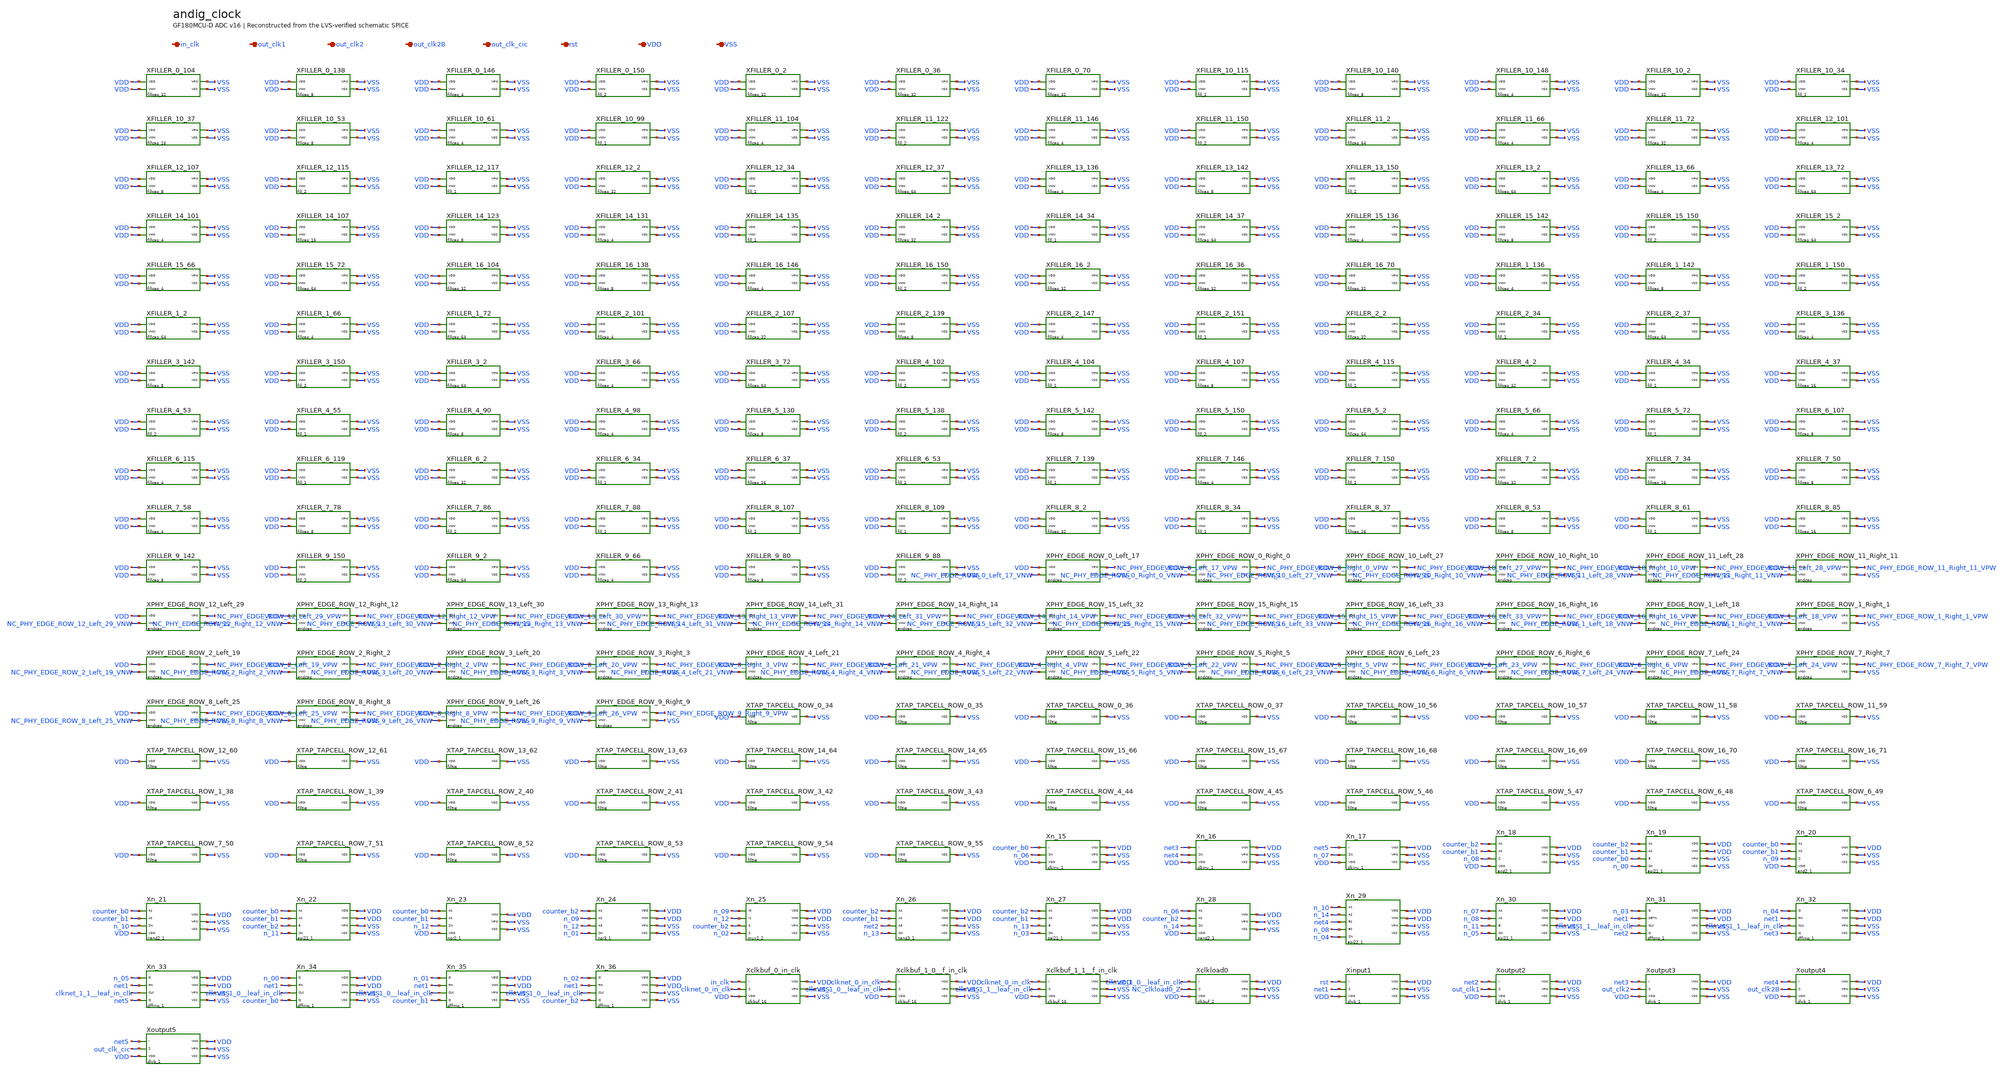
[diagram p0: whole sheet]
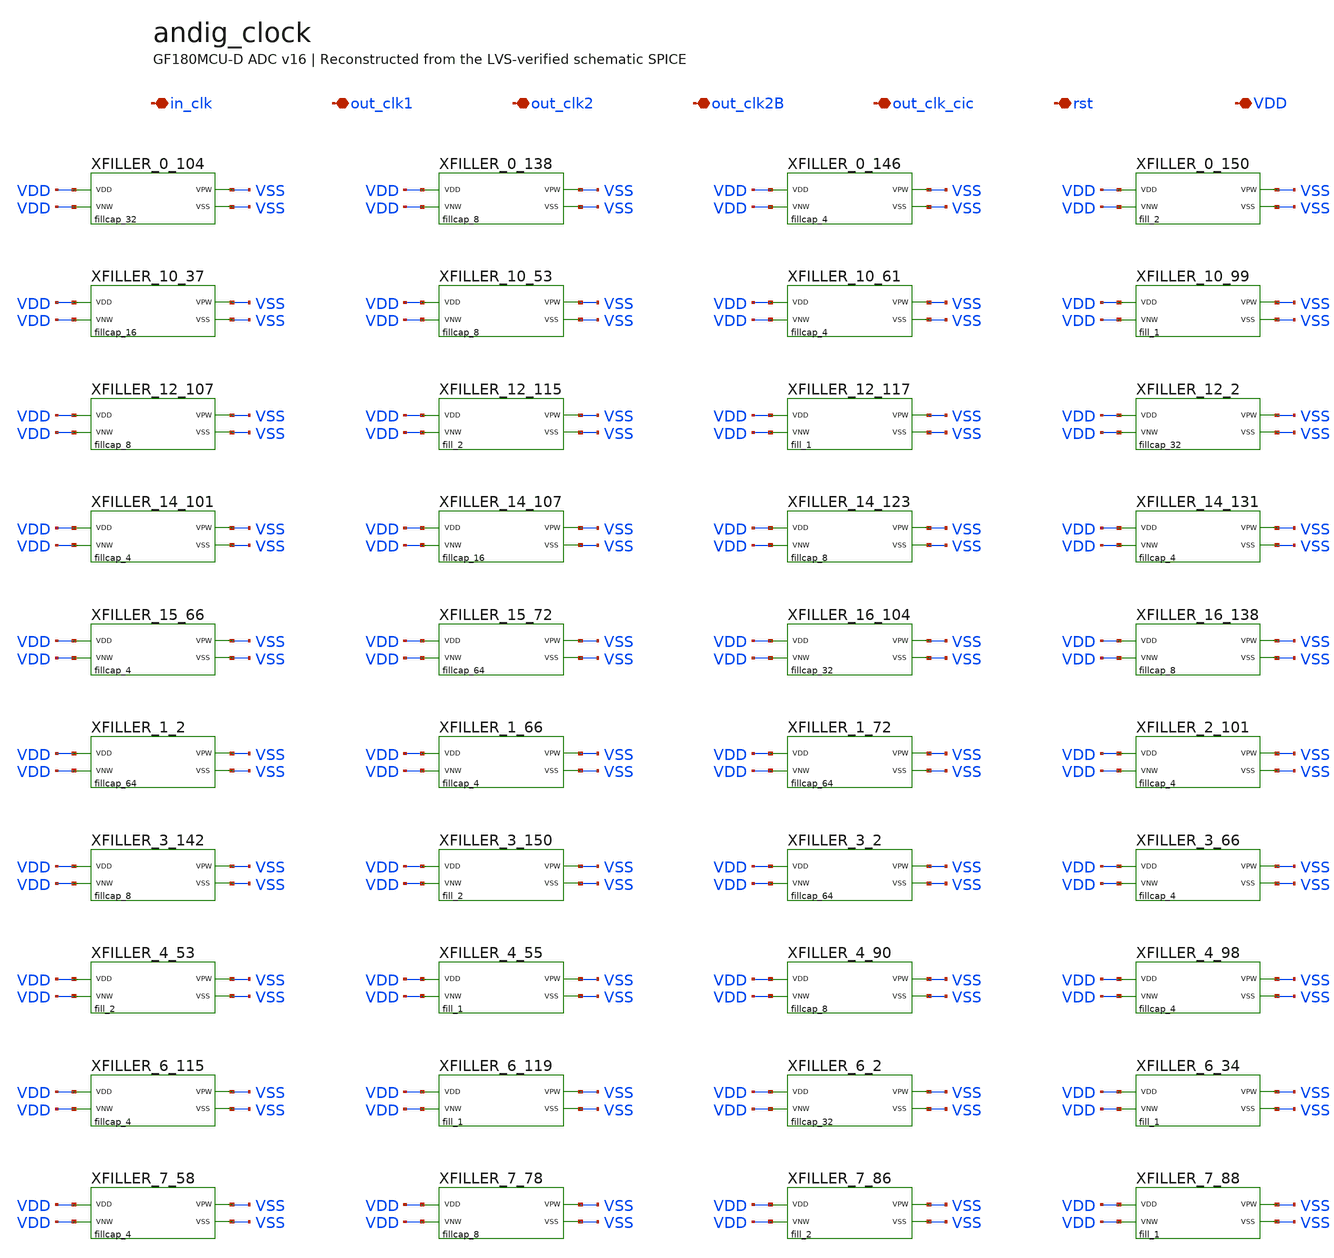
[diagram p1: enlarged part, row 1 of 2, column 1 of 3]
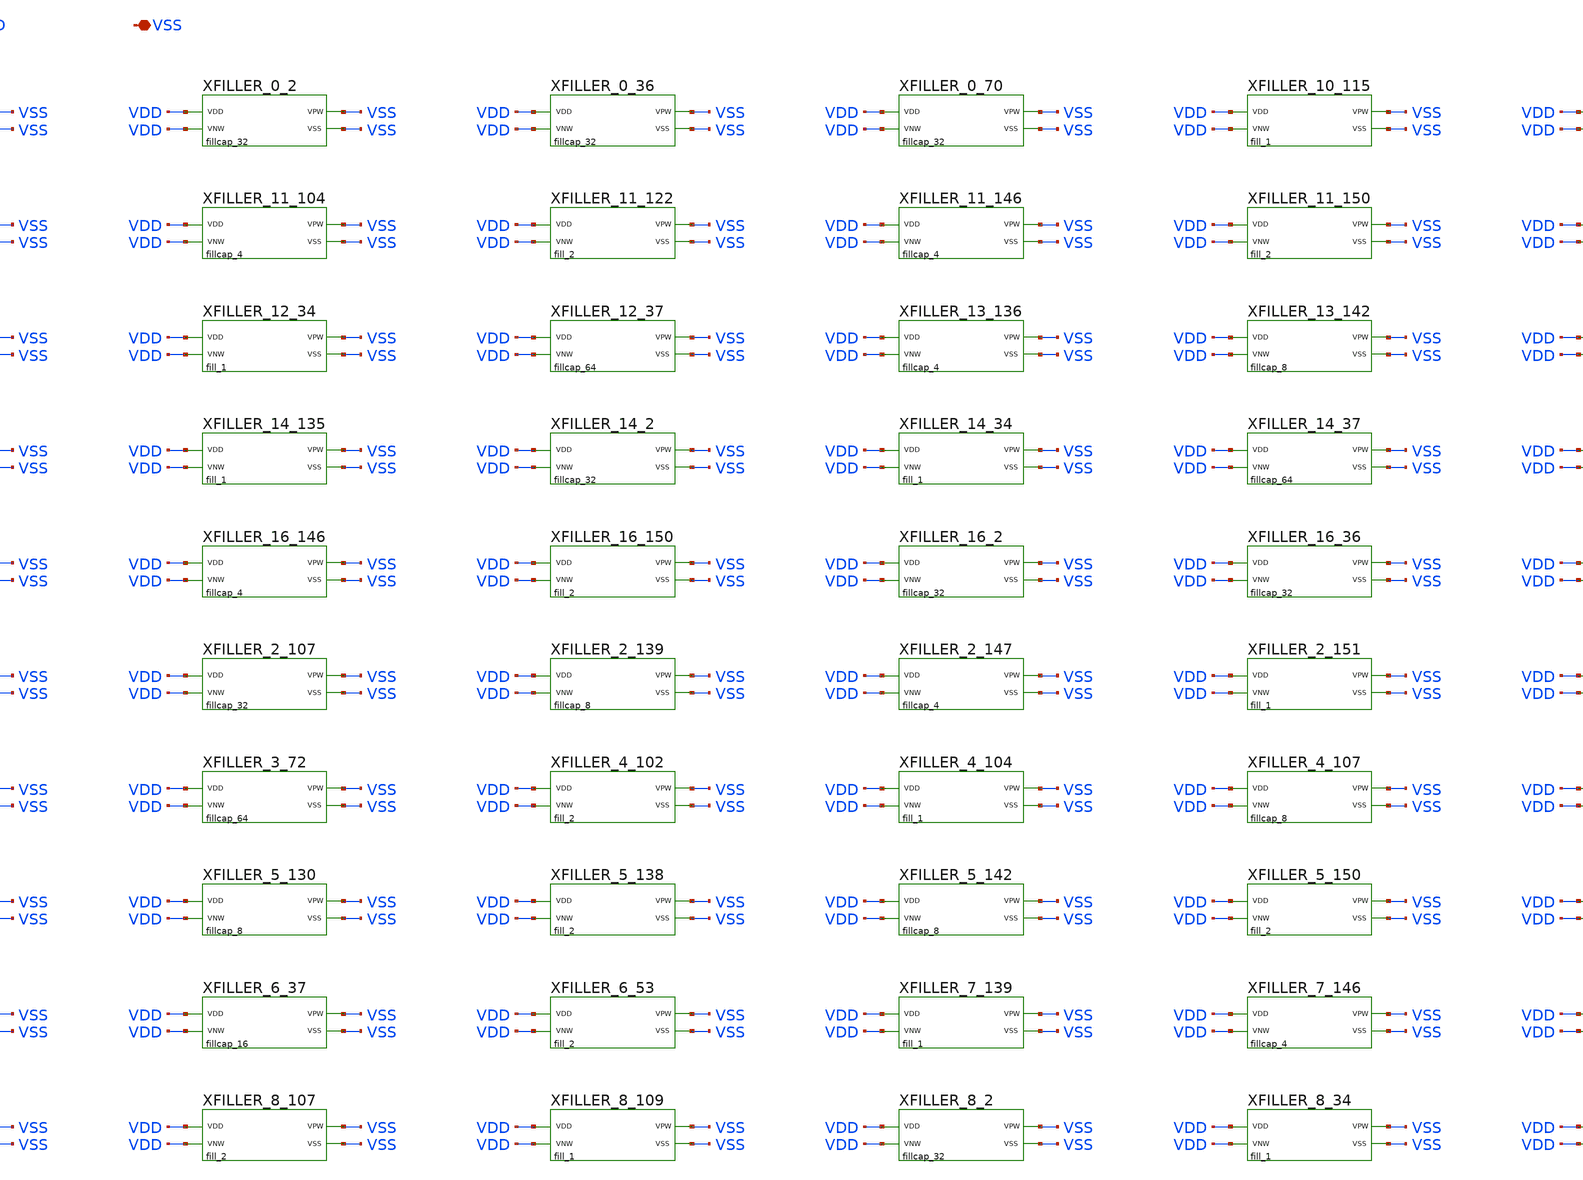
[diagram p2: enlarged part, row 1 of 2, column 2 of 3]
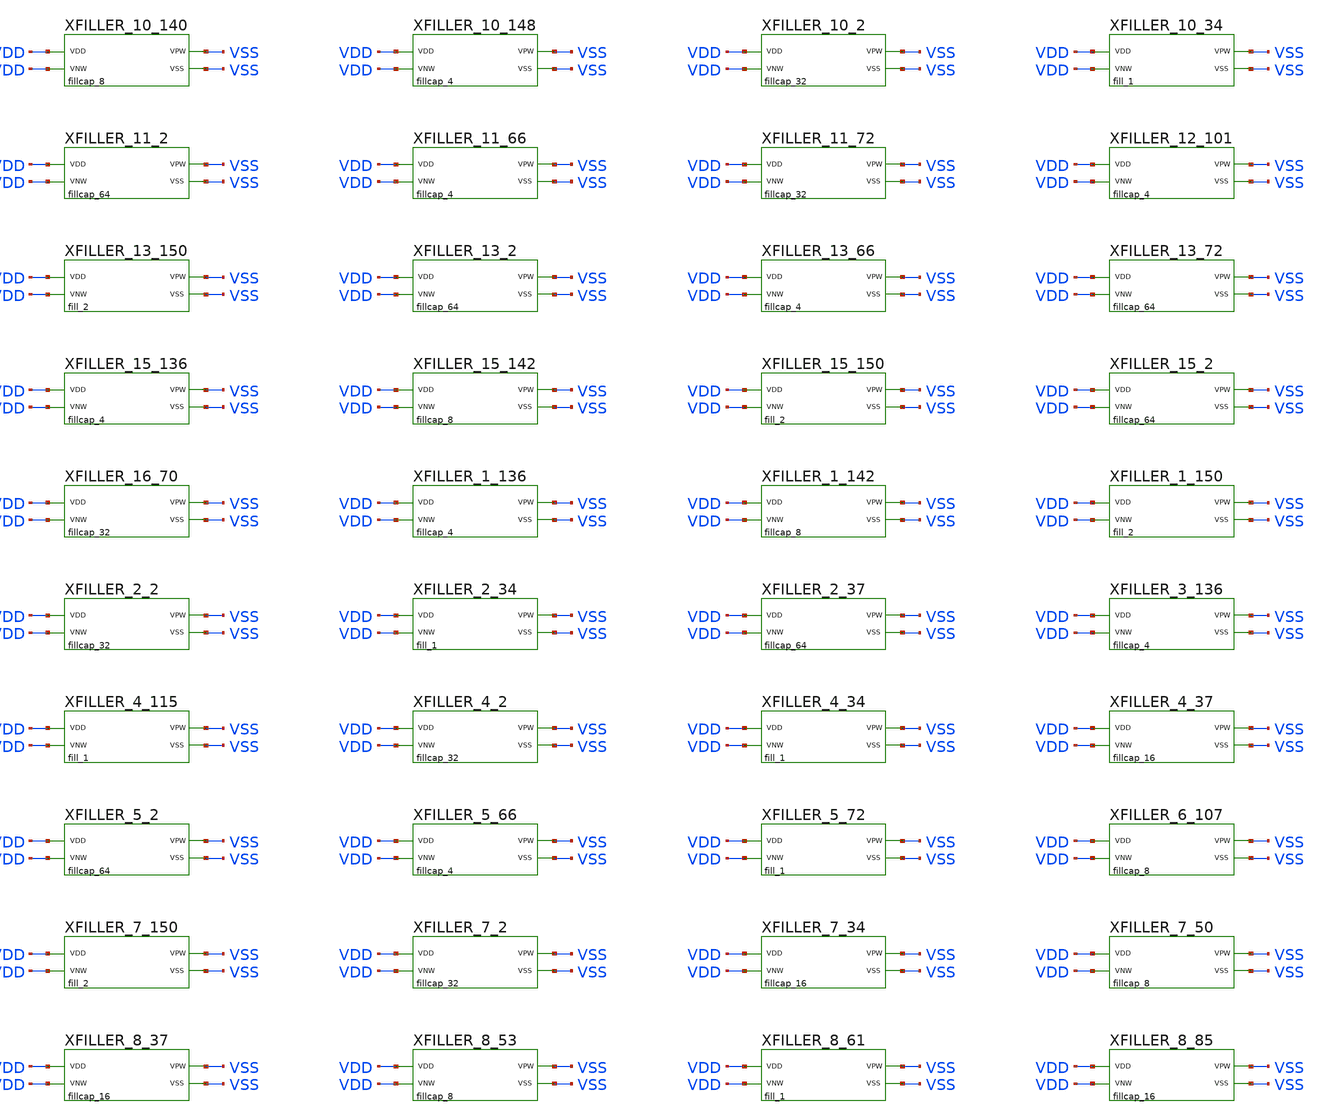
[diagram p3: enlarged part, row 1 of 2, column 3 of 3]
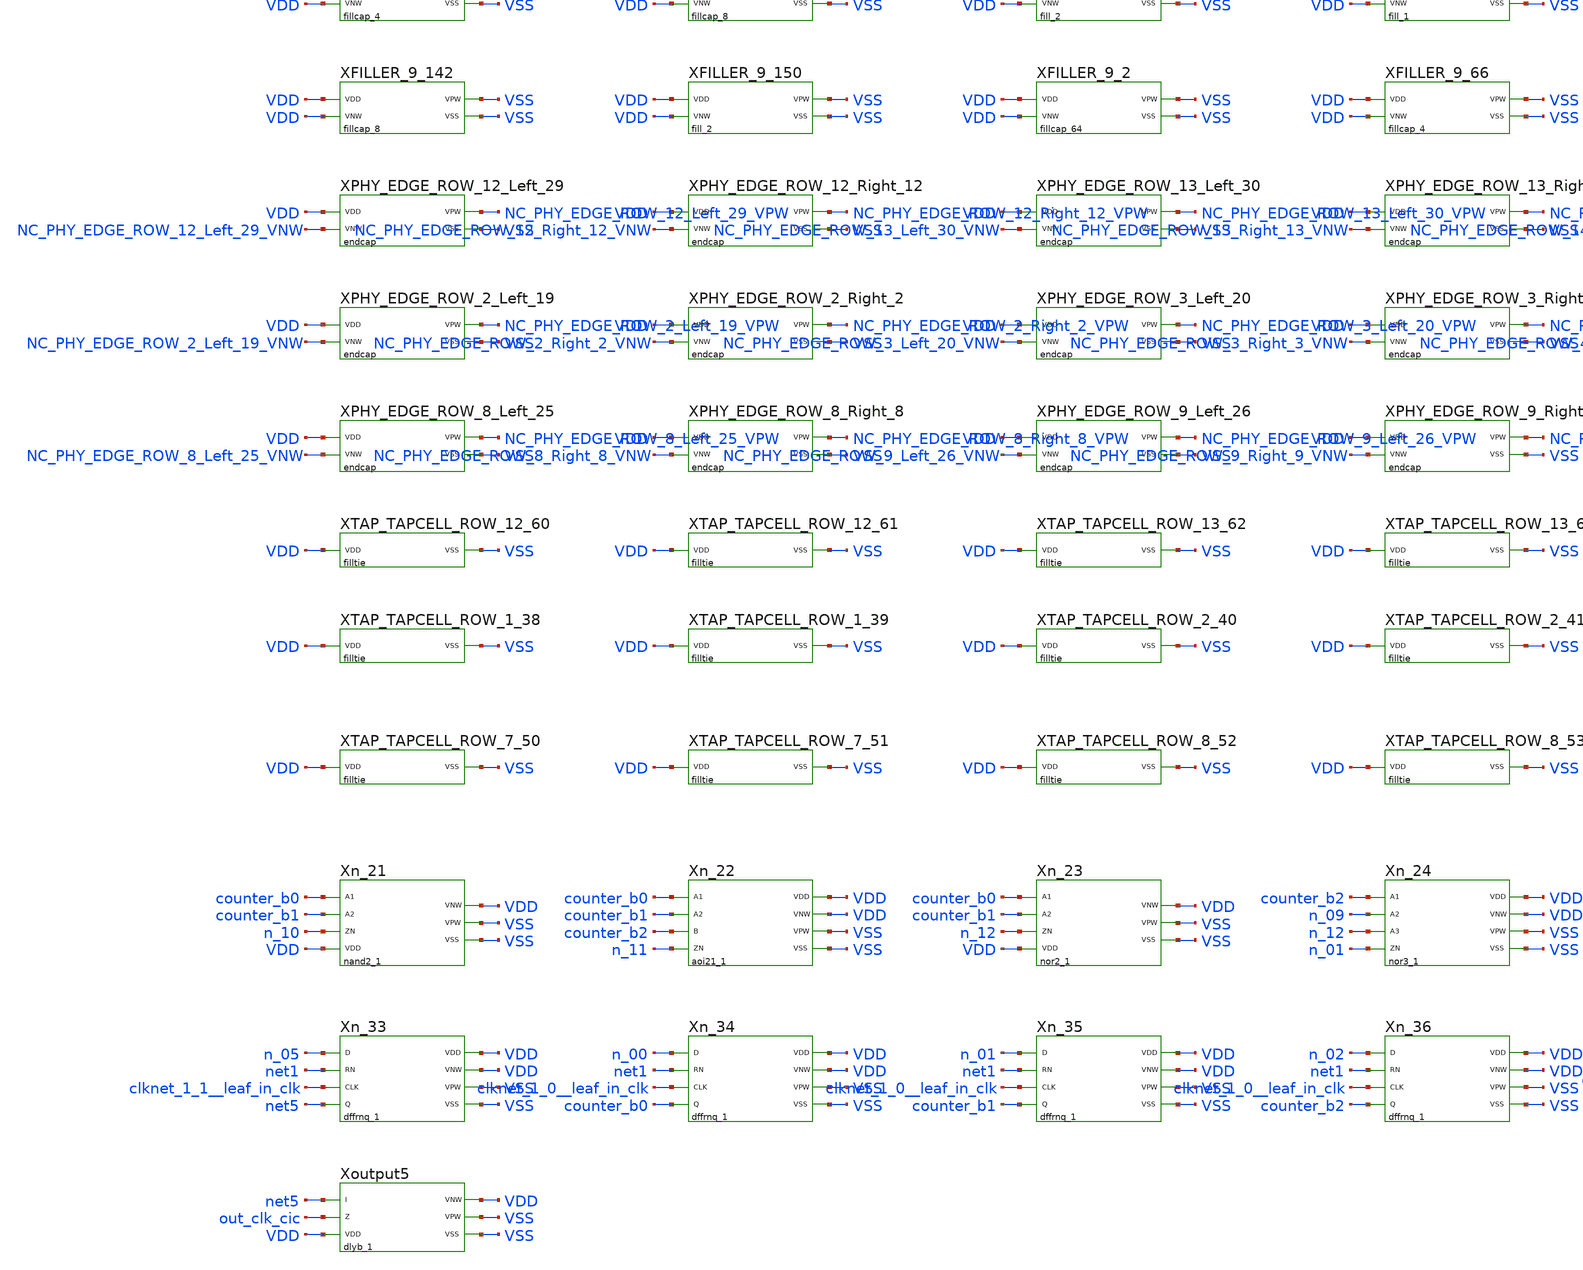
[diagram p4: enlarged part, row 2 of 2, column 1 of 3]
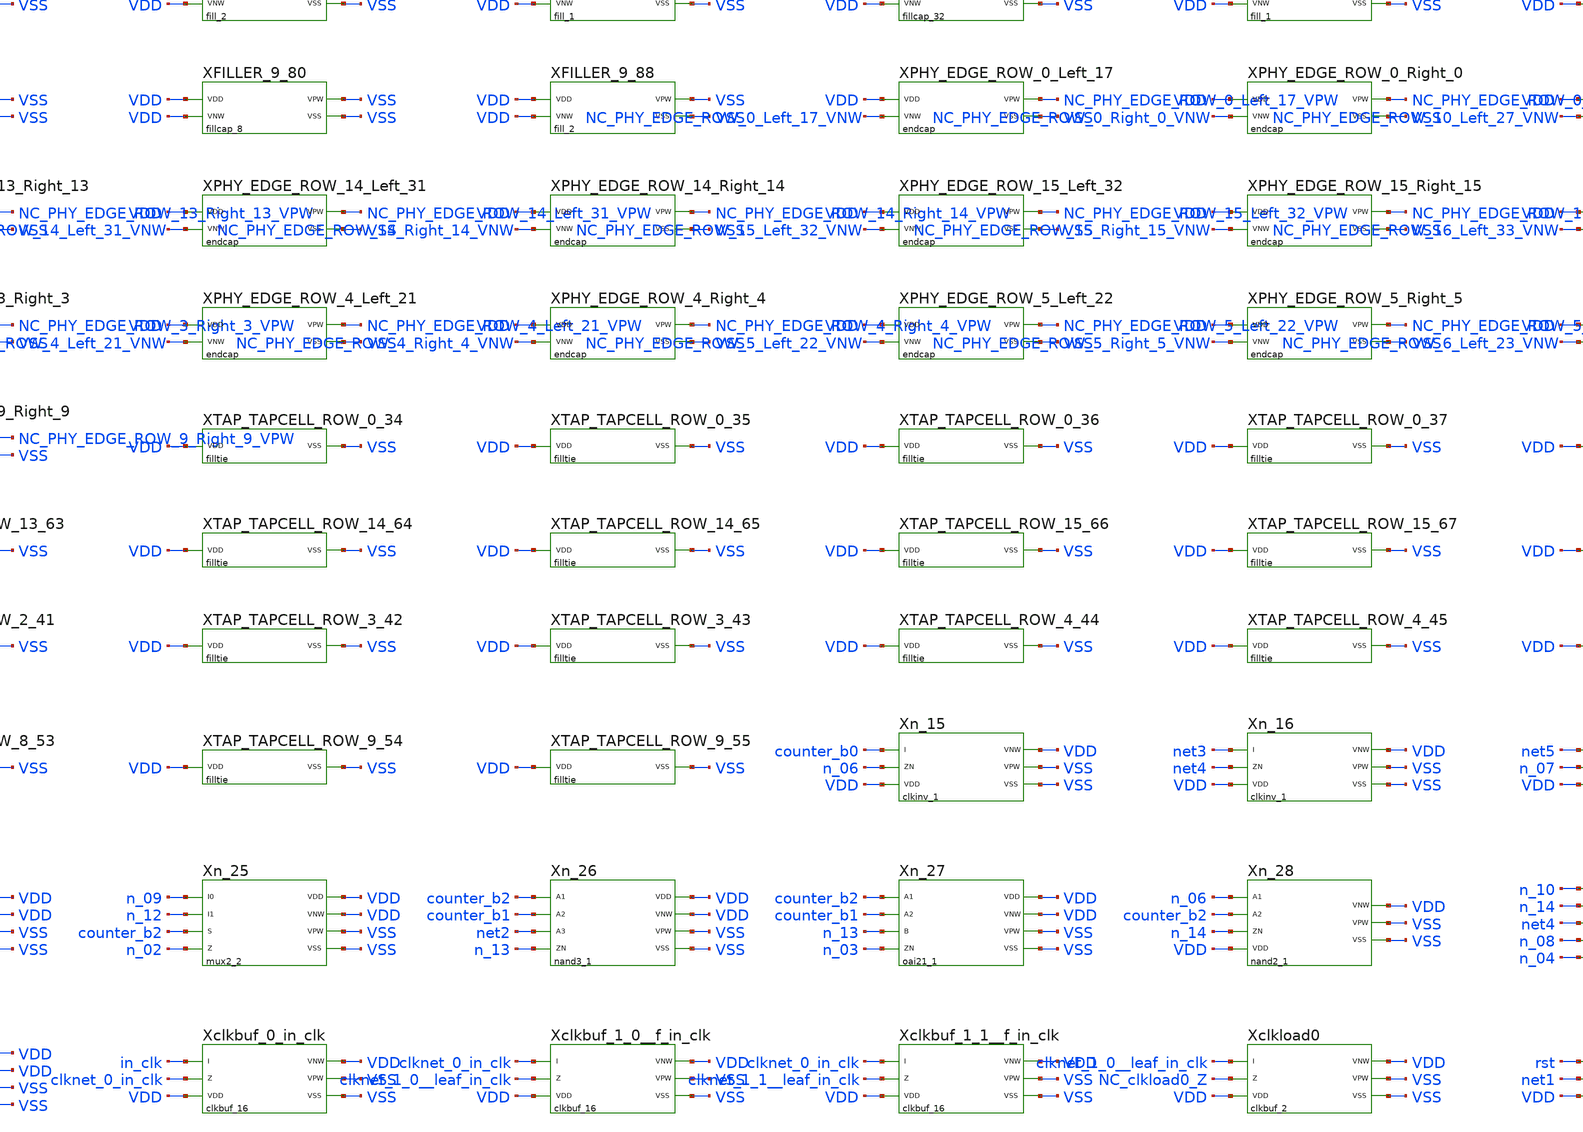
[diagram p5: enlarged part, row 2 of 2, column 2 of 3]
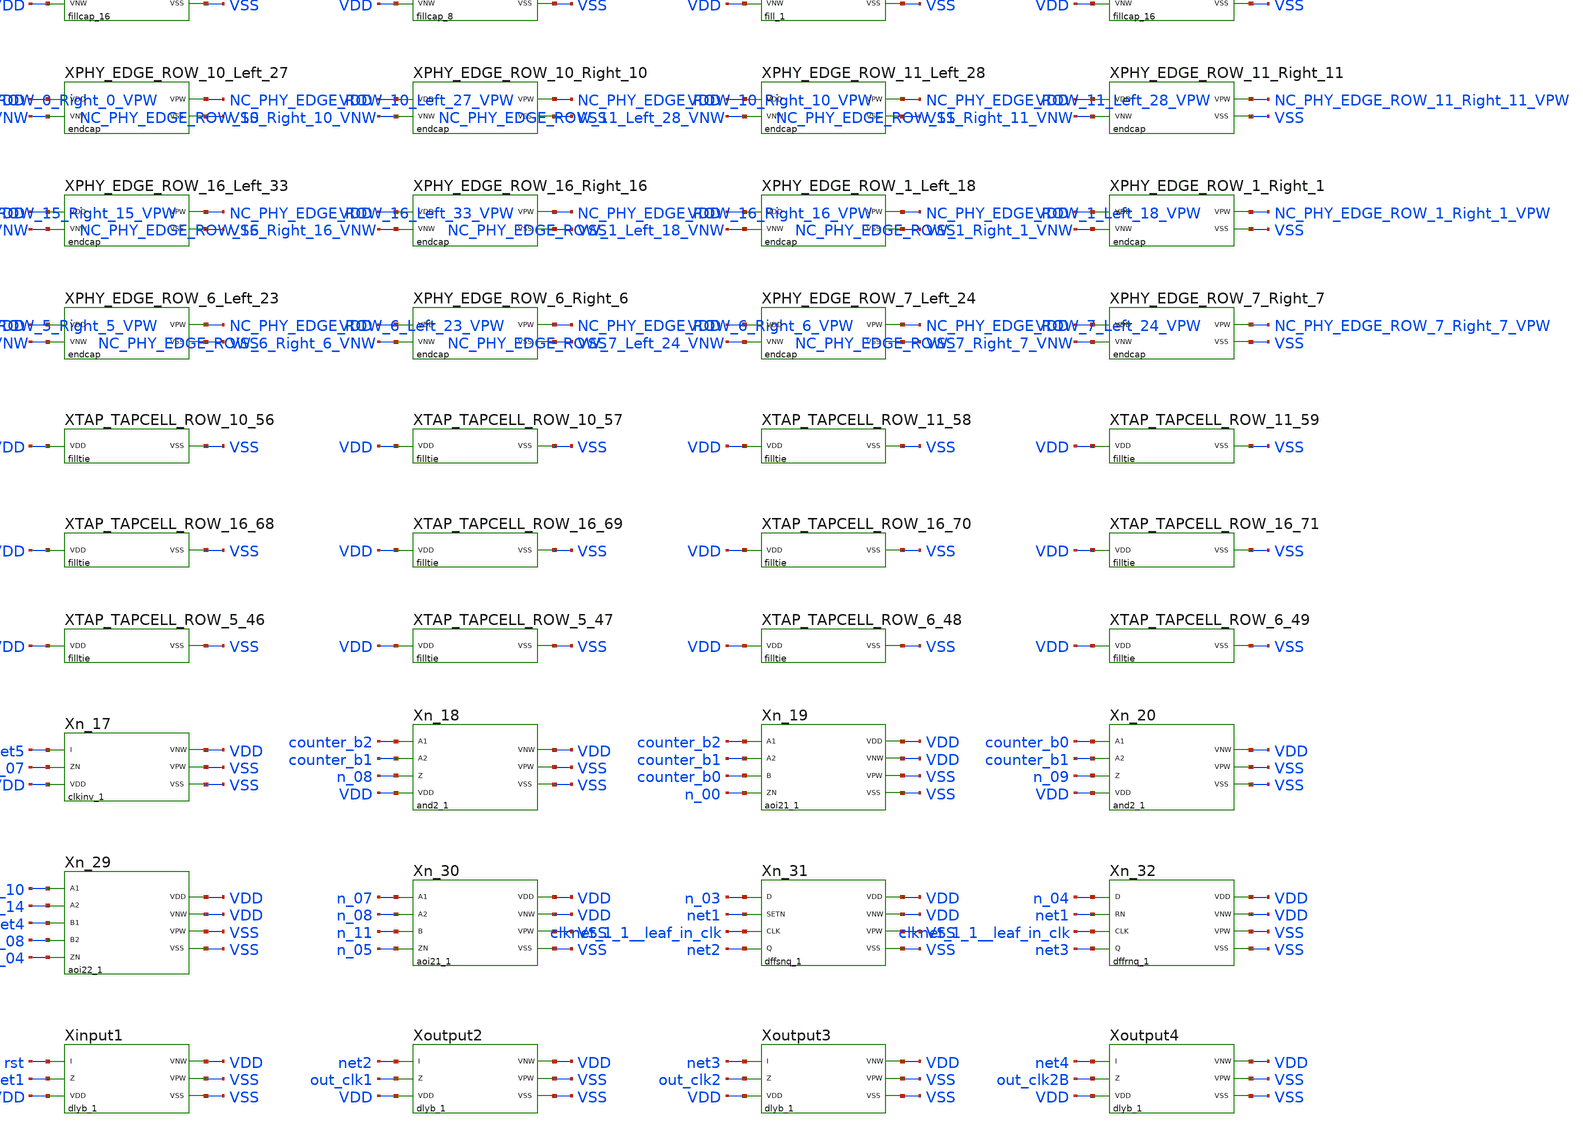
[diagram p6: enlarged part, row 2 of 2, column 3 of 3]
** sch_path: src/schematics/INTEGRATION/ADC_final/ADC_v17_Xschem/andig_clock.sch
* Copyright (C) 1998-2026 Stefan Frederik Schippers
* This program is free software; you can redistribute it and/or modify
* it under the terms of the GNU General Public License as published by
* the Free Software Foundation; either version 2 of the License, or
* (at your option) any later version.
**.subckt andig_clock in_clk out_clk1 out_clk2 out_clk2B out_clk_cic rst VDD VSS
*.iopin in_clk
*.iopin out_clk1
*.iopin out_clk2
*.iopin out_clk2B
*.iopin out_clk_cic
*.iopin rst
*.iopin VDD
*.iopin VSS
XFILLER_0_104 VDD VDD VSS VSS gf180mcu_fd_sc_mcu7t5v0__fillcap_32
XFILLER_0_138 VDD VDD VSS VSS gf180mcu_fd_sc_mcu7t5v0__fillcap_8
XFILLER_0_146 VDD VDD VSS VSS gf180mcu_fd_sc_mcu7t5v0__fillcap_4
XFILLER_0_150 VDD VDD VSS VSS gf180mcu_fd_sc_mcu7t5v0__fill_2
XFILLER_0_2 VDD VDD VSS VSS gf180mcu_fd_sc_mcu7t5v0__fillcap_32
XFILLER_0_36 VDD VDD VSS VSS gf180mcu_fd_sc_mcu7t5v0__fillcap_32
XFILLER_0_70 VDD VDD VSS VSS gf180mcu_fd_sc_mcu7t5v0__fillcap_32
XFILLER_10_115 VDD VDD VSS VSS gf180mcu_fd_sc_mcu7t5v0__fill_1
XFILLER_10_140 VDD VDD VSS VSS gf180mcu_fd_sc_mcu7t5v0__fillcap_8
XFILLER_10_148 VDD VDD VSS VSS gf180mcu_fd_sc_mcu7t5v0__fillcap_4
XFILLER_10_2 VDD VDD VSS VSS gf180mcu_fd_sc_mcu7t5v0__fillcap_32
XFILLER_10_34 VDD VDD VSS VSS gf180mcu_fd_sc_mcu7t5v0__fill_1
XFILLER_10_37 VDD VDD VSS VSS gf180mcu_fd_sc_mcu7t5v0__fillcap_16
XFILLER_10_53 VDD VDD VSS VSS gf180mcu_fd_sc_mcu7t5v0__fillcap_8
XFILLER_10_61 VDD VDD VSS VSS gf180mcu_fd_sc_mcu7t5v0__fillcap_4
XFILLER_10_99 VDD VDD VSS VSS gf180mcu_fd_sc_mcu7t5v0__fill_1
XFILLER_11_104 VDD VDD VSS VSS gf180mcu_fd_sc_mcu7t5v0__fillcap_4
XFILLER_11_122 VDD VDD VSS VSS gf180mcu_fd_sc_mcu7t5v0__fill_2
XFILLER_11_146 VDD VDD VSS VSS gf180mcu_fd_sc_mcu7t5v0__fillcap_4
XFILLER_11_150 VDD VDD VSS VSS gf180mcu_fd_sc_mcu7t5v0__fill_2
XFILLER_11_2 VDD VDD VSS VSS gf180mcu_fd_sc_mcu7t5v0__fillcap_64
XFILLER_11_66 VDD VDD VSS VSS gf180mcu_fd_sc_mcu7t5v0__fillcap_4
XFILLER_11_72 VDD VDD VSS VSS gf180mcu_fd_sc_mcu7t5v0__fillcap_32
XFILLER_12_101 VDD VDD VSS VSS gf180mcu_fd_sc_mcu7t5v0__fillcap_4
XFILLER_12_107 VDD VDD VSS VSS gf180mcu_fd_sc_mcu7t5v0__fillcap_8
XFILLER_12_115 VDD VDD VSS VSS gf180mcu_fd_sc_mcu7t5v0__fill_2
XFILLER_12_117 VDD VDD VSS VSS gf180mcu_fd_sc_mcu7t5v0__fill_1
XFILLER_12_2 VDD VDD VSS VSS gf180mcu_fd_sc_mcu7t5v0__fillcap_32
XFILLER_12_34 VDD VDD VSS VSS gf180mcu_fd_sc_mcu7t5v0__fill_1
XFILLER_12_37 VDD VDD VSS VSS gf180mcu_fd_sc_mcu7t5v0__fillcap_64
XFILLER_13_136 VDD VDD VSS VSS gf180mcu_fd_sc_mcu7t5v0__fillcap_4
XFILLER_13_142 VDD VDD VSS VSS gf180mcu_fd_sc_mcu7t5v0__fillcap_8
XFILLER_13_150 VDD VDD VSS VSS gf180mcu_fd_sc_mcu7t5v0__fill_2
XFILLER_13_2 VDD VDD VSS VSS gf180mcu_fd_sc_mcu7t5v0__fillcap_64
XFILLER_13_66 VDD VDD VSS VSS gf180mcu_fd_sc_mcu7t5v0__fillcap_4
XFILLER_13_72 VDD VDD VSS VSS gf180mcu_fd_sc_mcu7t5v0__fillcap_64
XFILLER_14_101 VDD VDD VSS VSS gf180mcu_fd_sc_mcu7t5v0__fillcap_4
XFILLER_14_107 VDD VDD VSS VSS gf180mcu_fd_sc_mcu7t5v0__fillcap_16
XFILLER_14_123 VDD VDD VSS VSS gf180mcu_fd_sc_mcu7t5v0__fillcap_8
XFILLER_14_131 VDD VDD VSS VSS gf180mcu_fd_sc_mcu7t5v0__fillcap_4
XFILLER_14_135 VDD VDD VSS VSS gf180mcu_fd_sc_mcu7t5v0__fill_1
XFILLER_14_2 VDD VDD VSS VSS gf180mcu_fd_sc_mcu7t5v0__fillcap_32
XFILLER_14_34 VDD VDD VSS VSS gf180mcu_fd_sc_mcu7t5v0__fill_1
XFILLER_14_37 VDD VDD VSS VSS gf180mcu_fd_sc_mcu7t5v0__fillcap_64
XFILLER_15_136 VDD VDD VSS VSS gf180mcu_fd_sc_mcu7t5v0__fillcap_4
XFILLER_15_142 VDD VDD VSS VSS gf180mcu_fd_sc_mcu7t5v0__fillcap_8
XFILLER_15_150 VDD VDD VSS VSS gf180mcu_fd_sc_mcu7t5v0__fill_2
XFILLER_15_2 VDD VDD VSS VSS gf180mcu_fd_sc_mcu7t5v0__fillcap_64
XFILLER_15_66 VDD VDD VSS VSS gf180mcu_fd_sc_mcu7t5v0__fillcap_4
XFILLER_15_72 VDD VDD VSS VSS gf180mcu_fd_sc_mcu7t5v0__fillcap_64
XFILLER_16_104 VDD VDD VSS VSS gf180mcu_fd_sc_mcu7t5v0__fillcap_32
XFILLER_16_138 VDD VDD VSS VSS gf180mcu_fd_sc_mcu7t5v0__fillcap_8
XFILLER_16_146 VDD VDD VSS VSS gf180mcu_fd_sc_mcu7t5v0__fillcap_4
XFILLER_16_150 VDD VDD VSS VSS gf180mcu_fd_sc_mcu7t5v0__fill_2
XFILLER_16_2 VDD VDD VSS VSS gf180mcu_fd_sc_mcu7t5v0__fillcap_32
XFILLER_16_36 VDD VDD VSS VSS gf180mcu_fd_sc_mcu7t5v0__fillcap_32
XFILLER_16_70 VDD VDD VSS VSS gf180mcu_fd_sc_mcu7t5v0__fillcap_32
XFILLER_1_136 VDD VDD VSS VSS gf180mcu_fd_sc_mcu7t5v0__fillcap_4
XFILLER_1_142 VDD VDD VSS VSS gf180mcu_fd_sc_mcu7t5v0__fillcap_8
XFILLER_1_150 VDD VDD VSS VSS gf180mcu_fd_sc_mcu7t5v0__fill_2
XFILLER_1_2 VDD VDD VSS VSS gf180mcu_fd_sc_mcu7t5v0__fillcap_64
XFILLER_1_66 VDD VDD VSS VSS gf180mcu_fd_sc_mcu7t5v0__fillcap_4
XFILLER_1_72 VDD VDD VSS VSS gf180mcu_fd_sc_mcu7t5v0__fillcap_64
XFILLER_2_101 VDD VDD VSS VSS gf180mcu_fd_sc_mcu7t5v0__fillcap_4
XFILLER_2_107 VDD VDD VSS VSS gf180mcu_fd_sc_mcu7t5v0__fillcap_32
XFILLER_2_139 VDD VDD VSS VSS gf180mcu_fd_sc_mcu7t5v0__fillcap_8
XFILLER_2_147 VDD VDD VSS VSS gf180mcu_fd_sc_mcu7t5v0__fillcap_4
XFILLER_2_151 VDD VDD VSS VSS gf180mcu_fd_sc_mcu7t5v0__fill_1
XFILLER_2_2 VDD VDD VSS VSS gf180mcu_fd_sc_mcu7t5v0__fillcap_32
XFILLER_2_34 VDD VDD VSS VSS gf180mcu_fd_sc_mcu7t5v0__fill_1
XFILLER_2_37 VDD VDD VSS VSS gf180mcu_fd_sc_mcu7t5v0__fillcap_64
XFILLER_3_136 VDD VDD VSS VSS gf180mcu_fd_sc_mcu7t5v0__fillcap_4
XFILLER_3_142 VDD VDD VSS VSS gf180mcu_fd_sc_mcu7t5v0__fillcap_8
XFILLER_3_150 VDD VDD VSS VSS gf180mcu_fd_sc_mcu7t5v0__fill_2
XFILLER_3_2 VDD VDD VSS VSS gf180mcu_fd_sc_mcu7t5v0__fillcap_64
XFILLER_3_66 VDD VDD VSS VSS gf180mcu_fd_sc_mcu7t5v0__fillcap_4
XFILLER_3_72 VDD VDD VSS VSS gf180mcu_fd_sc_mcu7t5v0__fillcap_64
XFILLER_4_102 VDD VDD VSS VSS gf180mcu_fd_sc_mcu7t5v0__fill_2
XFILLER_4_104 VDD VDD VSS VSS gf180mcu_fd_sc_mcu7t5v0__fill_1
XFILLER_4_107 VDD VDD VSS VSS gf180mcu_fd_sc_mcu7t5v0__fillcap_8
XFILLER_4_115 VDD VDD VSS VSS gf180mcu_fd_sc_mcu7t5v0__fill_1
XFILLER_4_2 VDD VDD VSS VSS gf180mcu_fd_sc_mcu7t5v0__fillcap_32
XFILLER_4_34 VDD VDD VSS VSS gf180mcu_fd_sc_mcu7t5v0__fill_1
XFILLER_4_37 VDD VDD VSS VSS gf180mcu_fd_sc_mcu7t5v0__fillcap_16
XFILLER_4_53 VDD VDD VSS VSS gf180mcu_fd_sc_mcu7t5v0__fill_2
XFILLER_4_55 VDD VDD VSS VSS gf180mcu_fd_sc_mcu7t5v0__fill_1
XFILLER_4_90 VDD VDD VSS VSS gf180mcu_fd_sc_mcu7t5v0__fillcap_8
XFILLER_4_98 VDD VDD VSS VSS gf180mcu_fd_sc_mcu7t5v0__fillcap_4
XFILLER_5_130 VDD VDD VSS VSS gf180mcu_fd_sc_mcu7t5v0__fillcap_8
XFILLER_5_138 VDD VDD VSS VSS gf180mcu_fd_sc_mcu7t5v0__fill_2
XFILLER_5_142 VDD VDD VSS VSS gf180mcu_fd_sc_mcu7t5v0__fillcap_8
XFILLER_5_150 VDD VDD VSS VSS gf180mcu_fd_sc_mcu7t5v0__fill_2
XFILLER_5_2 VDD VDD VSS VSS gf180mcu_fd_sc_mcu7t5v0__fillcap_64
XFILLER_5_66 VDD VDD VSS VSS gf180mcu_fd_sc_mcu7t5v0__fillcap_4
XFILLER_5_72 VDD VDD VSS VSS gf180mcu_fd_sc_mcu7t5v0__fill_1
XFILLER_6_107 VDD VDD VSS VSS gf180mcu_fd_sc_mcu7t5v0__fillcap_8
XFILLER_6_115 VDD VDD VSS VSS gf180mcu_fd_sc_mcu7t5v0__fillcap_4
XFILLER_6_119 VDD VDD VSS VSS gf180mcu_fd_sc_mcu7t5v0__fill_1
XFILLER_6_2 VDD VDD VSS VSS gf180mcu_fd_sc_mcu7t5v0__fillcap_32
XFILLER_6_34 VDD VDD VSS VSS gf180mcu_fd_sc_mcu7t5v0__fill_1
XFILLER_6_37 VDD VDD VSS VSS gf180mcu_fd_sc_mcu7t5v0__fillcap_16
XFILLER_6_53 VDD VDD VSS VSS gf180mcu_fd_sc_mcu7t5v0__fill_2
XFILLER_7_139 VDD VDD VSS VSS gf180mcu_fd_sc_mcu7t5v0__fill_1
XFILLER_7_146 VDD VDD VSS VSS gf180mcu_fd_sc_mcu7t5v0__fillcap_4
XFILLER_7_150 VDD VDD VSS VSS gf180mcu_fd_sc_mcu7t5v0__fill_2
XFILLER_7_2 VDD VDD VSS VSS gf180mcu_fd_sc_mcu7t5v0__fillcap_32
XFILLER_7_34 VDD VDD VSS VSS gf180mcu_fd_sc_mcu7t5v0__fillcap_16
XFILLER_7_50 VDD VDD VSS VSS gf180mcu_fd_sc_mcu7t5v0__fillcap_8
XFILLER_7_58 VDD VDD VSS VSS gf180mcu_fd_sc_mcu7t5v0__fillcap_4
XFILLER_7_78 VDD VDD VSS VSS gf180mcu_fd_sc_mcu7t5v0__fillcap_8
XFILLER_7_86 VDD VDD VSS VSS gf180mcu_fd_sc_mcu7t5v0__fill_2
XFILLER_7_88 VDD VDD VSS VSS gf180mcu_fd_sc_mcu7t5v0__fill_1
XFILLER_8_107 VDD VDD VSS VSS gf180mcu_fd_sc_mcu7t5v0__fill_2
XFILLER_8_109 VDD VDD VSS VSS gf180mcu_fd_sc_mcu7t5v0__fill_1
XFILLER_8_2 VDD VDD VSS VSS gf180mcu_fd_sc_mcu7t5v0__fillcap_32
XFILLER_8_34 VDD VDD VSS VSS gf180mcu_fd_sc_mcu7t5v0__fill_1
XFILLER_8_37 VDD VDD VSS VSS gf180mcu_fd_sc_mcu7t5v0__fillcap_16
XFILLER_8_53 VDD VDD VSS VSS gf180mcu_fd_sc_mcu7t5v0__fillcap_8
XFILLER_8_61 VDD VDD VSS VSS gf180mcu_fd_sc_mcu7t5v0__fill_1
XFILLER_8_85 VDD VDD VSS VSS gf180mcu_fd_sc_mcu7t5v0__fillcap_16
XFILLER_9_142 VDD VDD VSS VSS gf180mcu_fd_sc_mcu7t5v0__fillcap_8
XFILLER_9_150 VDD VDD VSS VSS gf180mcu_fd_sc_mcu7t5v0__fill_2
XFILLER_9_2 VDD VDD VSS VSS gf180mcu_fd_sc_mcu7t5v0__fillcap_64
XFILLER_9_66 VDD VDD VSS VSS gf180mcu_fd_sc_mcu7t5v0__fillcap_4
XFILLER_9_80 VDD VDD VSS VSS gf180mcu_fd_sc_mcu7t5v0__fillcap_8
XFILLER_9_88 VDD VDD VSS VSS gf180mcu_fd_sc_mcu7t5v0__fill_2
XPHY_EDGE_ROW_0_Left_17 VDD NC_PHY_EDGE_ROW_0_Left_17_VNW NC_PHY_EDGE_ROW_0_Left_17_VPW VSS
+ gf180mcu_fd_sc_mcu7t5v0__endcap
XPHY_EDGE_ROW_0_Right_0 VDD NC_PHY_EDGE_ROW_0_Right_0_VNW NC_PHY_EDGE_ROW_0_Right_0_VPW VSS
+ gf180mcu_fd_sc_mcu7t5v0__endcap
XPHY_EDGE_ROW_10_Left_27 VDD NC_PHY_EDGE_ROW_10_Left_27_VNW NC_PHY_EDGE_ROW_10_Left_27_VPW VSS
+ gf180mcu_fd_sc_mcu7t5v0__endcap
XPHY_EDGE_ROW_10_Right_10 VDD NC_PHY_EDGE_ROW_10_Right_10_VNW NC_PHY_EDGE_ROW_10_Right_10_VPW VSS
+ gf180mcu_fd_sc_mcu7t5v0__endcap
XPHY_EDGE_ROW_11_Left_28 VDD NC_PHY_EDGE_ROW_11_Left_28_VNW NC_PHY_EDGE_ROW_11_Left_28_VPW VSS
+ gf180mcu_fd_sc_mcu7t5v0__endcap
XPHY_EDGE_ROW_11_Right_11 VDD NC_PHY_EDGE_ROW_11_Right_11_VNW NC_PHY_EDGE_ROW_11_Right_11_VPW VSS
+ gf180mcu_fd_sc_mcu7t5v0__endcap
XPHY_EDGE_ROW_12_Left_29 VDD NC_PHY_EDGE_ROW_12_Left_29_VNW NC_PHY_EDGE_ROW_12_Left_29_VPW VSS
+ gf180mcu_fd_sc_mcu7t5v0__endcap
XPHY_EDGE_ROW_12_Right_12 VDD NC_PHY_EDGE_ROW_12_Right_12_VNW NC_PHY_EDGE_ROW_12_Right_12_VPW VSS
+ gf180mcu_fd_sc_mcu7t5v0__endcap
XPHY_EDGE_ROW_13_Left_30 VDD NC_PHY_EDGE_ROW_13_Left_30_VNW NC_PHY_EDGE_ROW_13_Left_30_VPW VSS
+ gf180mcu_fd_sc_mcu7t5v0__endcap
XPHY_EDGE_ROW_13_Right_13 VDD NC_PHY_EDGE_ROW_13_Right_13_VNW NC_PHY_EDGE_ROW_13_Right_13_VPW VSS
+ gf180mcu_fd_sc_mcu7t5v0__endcap
XPHY_EDGE_ROW_14_Left_31 VDD NC_PHY_EDGE_ROW_14_Left_31_VNW NC_PHY_EDGE_ROW_14_Left_31_VPW VSS
+ gf180mcu_fd_sc_mcu7t5v0__endcap
XPHY_EDGE_ROW_14_Right_14 VDD NC_PHY_EDGE_ROW_14_Right_14_VNW NC_PHY_EDGE_ROW_14_Right_14_VPW VSS
+ gf180mcu_fd_sc_mcu7t5v0__endcap
XPHY_EDGE_ROW_15_Left_32 VDD NC_PHY_EDGE_ROW_15_Left_32_VNW NC_PHY_EDGE_ROW_15_Left_32_VPW VSS
+ gf180mcu_fd_sc_mcu7t5v0__endcap
XPHY_EDGE_ROW_15_Right_15 VDD NC_PHY_EDGE_ROW_15_Right_15_VNW NC_PHY_EDGE_ROW_15_Right_15_VPW VSS
+ gf180mcu_fd_sc_mcu7t5v0__endcap
XPHY_EDGE_ROW_16_Left_33 VDD NC_PHY_EDGE_ROW_16_Left_33_VNW NC_PHY_EDGE_ROW_16_Left_33_VPW VSS
+ gf180mcu_fd_sc_mcu7t5v0__endcap
XPHY_EDGE_ROW_16_Right_16 VDD NC_PHY_EDGE_ROW_16_Right_16_VNW NC_PHY_EDGE_ROW_16_Right_16_VPW VSS
+ gf180mcu_fd_sc_mcu7t5v0__endcap
XPHY_EDGE_ROW_1_Left_18 VDD NC_PHY_EDGE_ROW_1_Left_18_VNW NC_PHY_EDGE_ROW_1_Left_18_VPW VSS
+ gf180mcu_fd_sc_mcu7t5v0__endcap
XPHY_EDGE_ROW_1_Right_1 VDD NC_PHY_EDGE_ROW_1_Right_1_VNW NC_PHY_EDGE_ROW_1_Right_1_VPW VSS
+ gf180mcu_fd_sc_mcu7t5v0__endcap
XPHY_EDGE_ROW_2_Left_19 VDD NC_PHY_EDGE_ROW_2_Left_19_VNW NC_PHY_EDGE_ROW_2_Left_19_VPW VSS
+ gf180mcu_fd_sc_mcu7t5v0__endcap
XPHY_EDGE_ROW_2_Right_2 VDD NC_PHY_EDGE_ROW_2_Right_2_VNW NC_PHY_EDGE_ROW_2_Right_2_VPW VSS
+ gf180mcu_fd_sc_mcu7t5v0__endcap
XPHY_EDGE_ROW_3_Left_20 VDD NC_PHY_EDGE_ROW_3_Left_20_VNW NC_PHY_EDGE_ROW_3_Left_20_VPW VSS
+ gf180mcu_fd_sc_mcu7t5v0__endcap
XPHY_EDGE_ROW_3_Right_3 VDD NC_PHY_EDGE_ROW_3_Right_3_VNW NC_PHY_EDGE_ROW_3_Right_3_VPW VSS
+ gf180mcu_fd_sc_mcu7t5v0__endcap
XPHY_EDGE_ROW_4_Left_21 VDD NC_PHY_EDGE_ROW_4_Left_21_VNW NC_PHY_EDGE_ROW_4_Left_21_VPW VSS
+ gf180mcu_fd_sc_mcu7t5v0__endcap
XPHY_EDGE_ROW_4_Right_4 VDD NC_PHY_EDGE_ROW_4_Right_4_VNW NC_PHY_EDGE_ROW_4_Right_4_VPW VSS
+ gf180mcu_fd_sc_mcu7t5v0__endcap
XPHY_EDGE_ROW_5_Left_22 VDD NC_PHY_EDGE_ROW_5_Left_22_VNW NC_PHY_EDGE_ROW_5_Left_22_VPW VSS
+ gf180mcu_fd_sc_mcu7t5v0__endcap
XPHY_EDGE_ROW_5_Right_5 VDD NC_PHY_EDGE_ROW_5_Right_5_VNW NC_PHY_EDGE_ROW_5_Right_5_VPW VSS
+ gf180mcu_fd_sc_mcu7t5v0__endcap
XPHY_EDGE_ROW_6_Left_23 VDD NC_PHY_EDGE_ROW_6_Left_23_VNW NC_PHY_EDGE_ROW_6_Left_23_VPW VSS
+ gf180mcu_fd_sc_mcu7t5v0__endcap
XPHY_EDGE_ROW_6_Right_6 VDD NC_PHY_EDGE_ROW_6_Right_6_VNW NC_PHY_EDGE_ROW_6_Right_6_VPW VSS
+ gf180mcu_fd_sc_mcu7t5v0__endcap
XPHY_EDGE_ROW_7_Left_24 VDD NC_PHY_EDGE_ROW_7_Left_24_VNW NC_PHY_EDGE_ROW_7_Left_24_VPW VSS
+ gf180mcu_fd_sc_mcu7t5v0__endcap
XPHY_EDGE_ROW_7_Right_7 VDD NC_PHY_EDGE_ROW_7_Right_7_VNW NC_PHY_EDGE_ROW_7_Right_7_VPW VSS
+ gf180mcu_fd_sc_mcu7t5v0__endcap
XPHY_EDGE_ROW_8_Left_25 VDD NC_PHY_EDGE_ROW_8_Left_25_VNW NC_PHY_EDGE_ROW_8_Left_25_VPW VSS
+ gf180mcu_fd_sc_mcu7t5v0__endcap
XPHY_EDGE_ROW_8_Right_8 VDD NC_PHY_EDGE_ROW_8_Right_8_VNW NC_PHY_EDGE_ROW_8_Right_8_VPW VSS
+ gf180mcu_fd_sc_mcu7t5v0__endcap
XPHY_EDGE_ROW_9_Left_26 VDD NC_PHY_EDGE_ROW_9_Left_26_VNW NC_PHY_EDGE_ROW_9_Left_26_VPW VSS
+ gf180mcu_fd_sc_mcu7t5v0__endcap
XPHY_EDGE_ROW_9_Right_9 VDD NC_PHY_EDGE_ROW_9_Right_9_VNW NC_PHY_EDGE_ROW_9_Right_9_VPW VSS
+ gf180mcu_fd_sc_mcu7t5v0__endcap
XTAP_TAPCELL_ROW_0_34 VDD VSS gf180mcu_fd_sc_mcu7t5v0__filltie
XTAP_TAPCELL_ROW_0_35 VDD VSS gf180mcu_fd_sc_mcu7t5v0__filltie
XTAP_TAPCELL_ROW_0_36 VDD VSS gf180mcu_fd_sc_mcu7t5v0__filltie
XTAP_TAPCELL_ROW_0_37 VDD VSS gf180mcu_fd_sc_mcu7t5v0__filltie
XTAP_TAPCELL_ROW_10_56 VDD VSS gf180mcu_fd_sc_mcu7t5v0__filltie
XTAP_TAPCELL_ROW_10_57 VDD VSS gf180mcu_fd_sc_mcu7t5v0__filltie
XTAP_TAPCELL_ROW_11_58 VDD VSS gf180mcu_fd_sc_mcu7t5v0__filltie
XTAP_TAPCELL_ROW_11_59 VDD VSS gf180mcu_fd_sc_mcu7t5v0__filltie
XTAP_TAPCELL_ROW_12_60 VDD VSS gf180mcu_fd_sc_mcu7t5v0__filltie
XTAP_TAPCELL_ROW_12_61 VDD VSS gf180mcu_fd_sc_mcu7t5v0__filltie
XTAP_TAPCELL_ROW_13_62 VDD VSS gf180mcu_fd_sc_mcu7t5v0__filltie
XTAP_TAPCELL_ROW_13_63 VDD VSS gf180mcu_fd_sc_mcu7t5v0__filltie
XTAP_TAPCELL_ROW_14_64 VDD VSS gf180mcu_fd_sc_mcu7t5v0__filltie
XTAP_TAPCELL_ROW_14_65 VDD VSS gf180mcu_fd_sc_mcu7t5v0__filltie
XTAP_TAPCELL_ROW_15_66 VDD VSS gf180mcu_fd_sc_mcu7t5v0__filltie
XTAP_TAPCELL_ROW_15_67 VDD VSS gf180mcu_fd_sc_mcu7t5v0__filltie
XTAP_TAPCELL_ROW_16_68 VDD VSS gf180mcu_fd_sc_mcu7t5v0__filltie
XTAP_TAPCELL_ROW_16_69 VDD VSS gf180mcu_fd_sc_mcu7t5v0__filltie
XTAP_TAPCELL_ROW_16_70 VDD VSS gf180mcu_fd_sc_mcu7t5v0__filltie
XTAP_TAPCELL_ROW_16_71 VDD VSS gf180mcu_fd_sc_mcu7t5v0__filltie
XTAP_TAPCELL_ROW_1_38 VDD VSS gf180mcu_fd_sc_mcu7t5v0__filltie
XTAP_TAPCELL_ROW_1_39 VDD VSS gf180mcu_fd_sc_mcu7t5v0__filltie
XTAP_TAPCELL_ROW_2_40 VDD VSS gf180mcu_fd_sc_mcu7t5v0__filltie
XTAP_TAPCELL_ROW_2_41 VDD VSS gf180mcu_fd_sc_mcu7t5v0__filltie
XTAP_TAPCELL_ROW_3_42 VDD VSS gf180mcu_fd_sc_mcu7t5v0__filltie
XTAP_TAPCELL_ROW_3_43 VDD VSS gf180mcu_fd_sc_mcu7t5v0__filltie
XTAP_TAPCELL_ROW_4_44 VDD VSS gf180mcu_fd_sc_mcu7t5v0__filltie
XTAP_TAPCELL_ROW_4_45 VDD VSS gf180mcu_fd_sc_mcu7t5v0__filltie
XTAP_TAPCELL_ROW_5_46 VDD VSS gf180mcu_fd_sc_mcu7t5v0__filltie
XTAP_TAPCELL_ROW_5_47 VDD VSS gf180mcu_fd_sc_mcu7t5v0__filltie
XTAP_TAPCELL_ROW_6_48 VDD VSS gf180mcu_fd_sc_mcu7t5v0__filltie
XTAP_TAPCELL_ROW_6_49 VDD VSS gf180mcu_fd_sc_mcu7t5v0__filltie
XTAP_TAPCELL_ROW_7_50 VDD VSS gf180mcu_fd_sc_mcu7t5v0__filltie
XTAP_TAPCELL_ROW_7_51 VDD VSS gf180mcu_fd_sc_mcu7t5v0__filltie
XTAP_TAPCELL_ROW_8_52 VDD VSS gf180mcu_fd_sc_mcu7t5v0__filltie
XTAP_TAPCELL_ROW_8_53 VDD VSS gf180mcu_fd_sc_mcu7t5v0__filltie
XTAP_TAPCELL_ROW_9_54 VDD VSS gf180mcu_fd_sc_mcu7t5v0__filltie
XTAP_TAPCELL_ROW_9_55 VDD VSS gf180mcu_fd_sc_mcu7t5v0__filltie
Xn_15 counter_b0 n_06 VDD VDD VSS VSS gf180mcu_fd_sc_mcu7t5v0__clkinv_1
Xn_16 net3 net4 VDD VDD VSS VSS gf180mcu_fd_sc_mcu7t5v0__clkinv_1
Xn_17 net5 n_07 VDD VDD VSS VSS gf180mcu_fd_sc_mcu7t5v0__clkinv_1
Xn_18 counter_b2 counter_b1 n_08 VDD VDD VSS VSS gf180mcu_fd_sc_mcu7t5v0__and2_1
Xn_19 counter_b2 counter_b1 counter_b0 n_00 VDD VDD VSS VSS gf180mcu_fd_sc_mcu7t5v0__aoi21_1
Xn_20 counter_b0 counter_b1 n_09 VDD VDD VSS VSS gf180mcu_fd_sc_mcu7t5v0__and2_1
Xn_21 counter_b0 counter_b1 n_10 VDD VDD VSS VSS gf180mcu_fd_sc_mcu7t5v0__nand2_1
Xn_22 counter_b0 counter_b1 counter_b2 n_11 VDD VDD VSS VSS gf180mcu_fd_sc_mcu7t5v0__aoi21_1
Xn_23 counter_b0 counter_b1 n_12 VDD VDD VSS VSS gf180mcu_fd_sc_mcu7t5v0__nor2_1
Xn_24 counter_b2 n_09 n_12 n_01 VDD VDD VSS VSS gf180mcu_fd_sc_mcu7t5v0__nor3_1
Xn_25 n_09 n_12 counter_b2 n_02 VDD VDD VSS VSS gf180mcu_fd_sc_mcu7t5v0__mux2_2
Xn_26 counter_b2 counter_b1 net2 n_13 VDD VDD VSS VSS gf180mcu_fd_sc_mcu7t5v0__nand3_1
Xn_27 counter_b2 counter_b1 n_13 n_03 VDD VDD VSS VSS gf180mcu_fd_sc_mcu7t5v0__oai21_1
Xn_28 n_06 counter_b2 n_14 VDD VDD VSS VSS gf180mcu_fd_sc_mcu7t5v0__nand2_1
Xn_29 n_10 n_14 net4 n_08 n_04 VDD VDD VSS VSS gf180mcu_fd_sc_mcu7t5v0__aoi22_1
Xn_30 n_07 n_08 n_11 n_05 VDD VDD VSS VSS gf180mcu_fd_sc_mcu7t5v0__aoi21_1
Xn_31 n_03 net1 clknet_1_1__leaf_in_clk net2 VDD VDD VSS VSS gf180mcu_fd_sc_mcu7t5v0__dffsnq_1
Xn_32 n_04 net1 clknet_1_1__leaf_in_clk net3 VDD VDD VSS VSS gf180mcu_fd_sc_mcu7t5v0__dffrnq_1
Xn_33 n_05 net1 clknet_1_1__leaf_in_clk net5 VDD VDD VSS VSS gf180mcu_fd_sc_mcu7t5v0__dffrnq_1
Xn_34 n_00 net1 clknet_1_0__leaf_in_clk counter_b0 VDD VDD VSS VSS gf180mcu_fd_sc_mcu7t5v0__dffrnq_1
Xn_35 n_01 net1 clknet_1_0__leaf_in_clk counter_b1 VDD VDD VSS VSS gf180mcu_fd_sc_mcu7t5v0__dffrnq_1
Xn_36 n_02 net1 clknet_1_0__leaf_in_clk counter_b2 VDD VDD VSS VSS gf180mcu_fd_sc_mcu7t5v0__dffrnq_1
Xclkbuf_0_in_clk in_clk clknet_0_in_clk VDD VDD VSS VSS gf180mcu_fd_sc_mcu7t5v0__clkbuf_16
Xclkbuf_1_0__f_in_clk clknet_0_in_clk clknet_1_0__leaf_in_clk VDD VDD VSS VSS
+ gf180mcu_fd_sc_mcu7t5v0__clkbuf_16
Xclkbuf_1_1__f_in_clk clknet_0_in_clk clknet_1_1__leaf_in_clk VDD VDD VSS VSS
+ gf180mcu_fd_sc_mcu7t5v0__clkbuf_16
Xclkload0 clknet_1_0__leaf_in_clk NC_clkload0_Z VDD VDD VSS VSS gf180mcu_fd_sc_mcu7t5v0__clkbuf_2
Xinput1 rst net1 VDD VDD VSS VSS gf180mcu_fd_sc_mcu7t5v0__dlyb_1
Xoutput2 net2 out_clk1 VDD VDD VSS VSS gf180mcu_fd_sc_mcu7t5v0__dlyb_1
Xoutput3 net3 out_clk2 VDD VDD VSS VSS gf180mcu_fd_sc_mcu7t5v0__dlyb_1
Xoutput4 net4 out_clk2B VDD VDD VSS VSS gf180mcu_fd_sc_mcu7t5v0__dlyb_1
Xoutput5 net5 out_clk_cic VDD VDD VSS VSS gf180mcu_fd_sc_mcu7t5v0__dlyb_1
**.ends
.end
